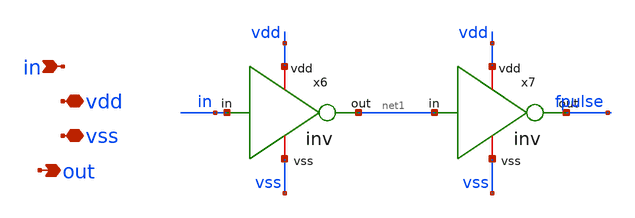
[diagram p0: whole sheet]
** sch_path: DESIGN/DACFUTURE_EDU/divider/divider.sch
**.subckt divider in vdd vss out
*.ipin in
*.iopin vdd
*.iopin vss
*.opin out
x6 in net1 vdd vss inv
x7 net1 fpulse vdd vss inv
**.ends
.end
